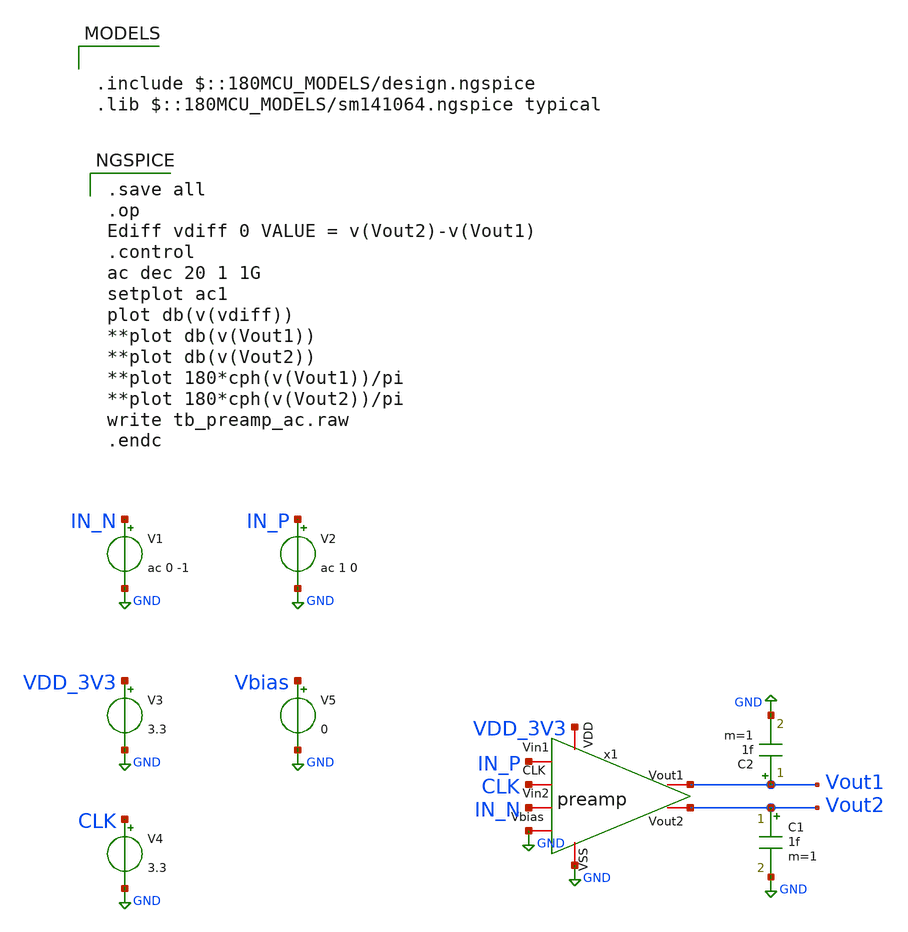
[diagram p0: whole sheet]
** sch_path: designs/comparator/preamp/tb_preamp_ac.sch
**.subckt tb_preamp_ac
x1 VDD_3V3 Vout2 Vout1 IN_N IN_P CLK GND GND preamp
V1 IN_N GND ac 0 -1
V3 VDD_3V3 GND 3.3
V4 CLK GND 3.3
V2 IN_P GND ac 1 0
C1 Vout2 GND 1f m=1
C2 Vout1 GND 1f m=1
V5 Vbias GND 0
**** begin user architecture code

.include $::180MCU_MODELS/design.ngspice
.lib $::180MCU_MODELS/sm141064.ngspice typical


.save all
.op
Ediff vdiff 0 VALUE = v(Vout2)-v(Vout1)
.control
ac dec 20 1 1G
setplot ac1
plot db(v(vdiff))
**plot db(v(Vout1))
**plot db(v(Vout2))
**plot 180*cph(v(Vout1))/pi
**plot 180*cph(v(Vout2))/pi
write tb_preamp_ac.raw
.endc

**** end user architecture code
**.ends

* expanding   symbol:  preamp.sym # of pins=8
** sym_path: designs/comparator/preamp/preamp.sym
** sch_path: designs/comparator/preamp/preamp.sch
.subckt preamp VDD Vout2 Vout1 Vin2 Vin1 CLK VSS Vbias
*.iopin VSS
*.iopin VDD
*.iopin Vout1
*.iopin Vout2
*.iopin Vin1
*.iopin Vin2
*.iopin CLK
*.iopin Vbias
XM1 Vout1 Vbias VDD VDD pfet_03v3 L=2u W=17u nf=1 ad='int((nf+1)/2) * W/nf * 0.18u' as='int((nf+2)/2) * W/nf * 0.18u'
+ pd='2*int((nf+1)/2) * (W/nf + 0.18u)' ps='2*int((nf+2)/2) * (W/nf + 0.18u)' nrd='0.18u / W' nrs='0.18u / W'
+ sa=0 sb=0 sd=0 m=1
XM2 Vout2 Vbias VDD VDD pfet_03v3 L=2u W=17u nf=1 ad='int((nf+1)/2) * W/nf * 0.18u' as='int((nf+2)/2) * W/nf * 0.18u'
+ pd='2*int((nf+1)/2) * (W/nf + 0.18u)' ps='2*int((nf+2)/2) * (W/nf + 0.18u)' nrd='0.18u / W' nrs='0.18u / W'
+ sa=0 sb=0 sd=0 m=1
XM3 Vout1 Vin1 net1 VSS nfet_03v3 L=2u W=10u nf=2 ad='int((nf+1)/2) * W/nf * 0.18u' as='int((nf+2)/2) * W/nf * 0.18u'
+ pd='2*int((nf+1)/2) * (W/nf + 0.18u)' ps='2*int((nf+2)/2) * (W/nf + 0.18u)' nrd='0.18u / W' nrs='0.18u / W'
+ sa=0 sb=0 sd=0 m=10
XM4 Vout2 Vin2 net1 VSS nfet_03v3 L=2u W=10u nf=2 ad='int((nf+1)/2) * W/nf * 0.18u' as='int((nf+2)/2) * W/nf * 0.18u'
+ pd='2*int((nf+1)/2) * (W/nf + 0.18u)' ps='2*int((nf+2)/2) * (W/nf + 0.18u)' nrd='0.18u / W' nrs='0.18u / W'
+ sa=0 sb=0 sd=0 m=10
XM5 net1 CLK VSS net2 nfet_03v3 L=2u W=15u nf=3 ad='int((nf+1)/2) * W/nf * 0.18u' as='int((nf+2)/2) * W/nf * 0.18u'
+ pd='2*int((nf+1)/2) * (W/nf + 0.18u)' ps='2*int((nf+2)/2) * (W/nf + 0.18u)' nrd='0.18u / W' nrs='0.18u / W'
+ sa=0 sb=0 sd=0 m=8
.ends

.GLOBAL GND
.end
